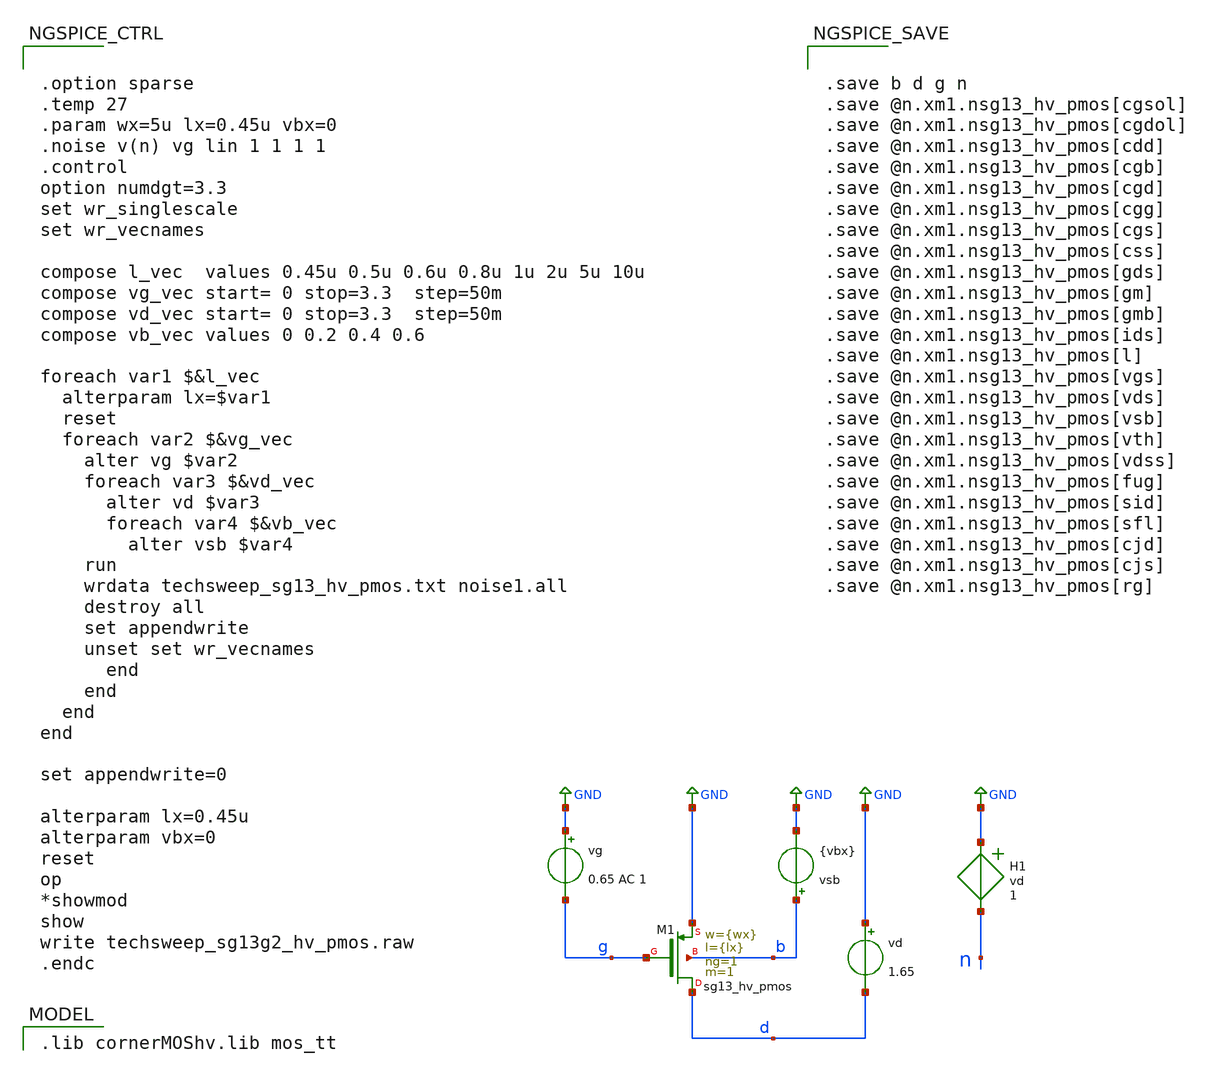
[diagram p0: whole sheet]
** sch_path: 3_real_circuits/techsweep_sg13g2_hv_pmos_test.sch
**.subckt techsweep_sg13g2_hv_pmos_test
XM1 d g GND b sg13_hv_pmos w={wx} l={lx} ng=1 m=1 mm_ok=1
vd GND d 1.65
vsb b GND {vbx}
vg GND g 0.65 AC 1
H1 GND n vd 1
**** begin user architecture code
 .lib cornerMOShv.lib mos_tt



.save b d g n
.save @n.xm1.nsg13_hv_pmos[cgsol]
.save @n.xm1.nsg13_hv_pmos[cgdol]
.save @n.xm1.nsg13_hv_pmos[cdd]
.save @n.xm1.nsg13_hv_pmos[cgb]
.save @n.xm1.nsg13_hv_pmos[cgd]
.save @n.xm1.nsg13_hv_pmos[cgg]
.save @n.xm1.nsg13_hv_pmos[cgs]
.save @n.xm1.nsg13_hv_pmos[css]
.save @n.xm1.nsg13_hv_pmos[gds]
.save @n.xm1.nsg13_hv_pmos[gm]
.save @n.xm1.nsg13_hv_pmos[gmb]
.save @n.xm1.nsg13_hv_pmos[ids]
.save @n.xm1.nsg13_hv_pmos[l]
.save @n.xm1.nsg13_hv_pmos[vgs]
.save @n.xm1.nsg13_hv_pmos[vds]
.save @n.xm1.nsg13_hv_pmos[vsb]
.save @n.xm1.nsg13_hv_pmos[vth]
.save @n.xm1.nsg13_hv_pmos[vdss]
.save @n.xm1.nsg13_hv_pmos[fug]
.save @n.xm1.nsg13_hv_pmos[sid]
.save @n.xm1.nsg13_hv_pmos[sfl]
.save @n.xm1.nsg13_hv_pmos[cjd]
.save @n.xm1.nsg13_hv_pmos[cjs]
.save @n.xm1.nsg13_hv_pmos[rg]




.option sparse
.temp 27
.param wx=5u lx=0.45u vbx=0
.noise v(n) vg lin 1 1 1 1
.control
option numdgt=3.3
set wr_singlescale
set wr_vecnames

compose l_vec  values 0.45u 0.5u 0.6u 0.8u 1u 2u 5u 10u
compose vg_vec start= 0 stop=3.3  step=50m
compose vd_vec start= 0 stop=3.3  step=50m
compose vb_vec values 0 0.2 0.4 0.6

foreach var1 $&l_vec
  alterparam lx=$var1
  reset
  foreach var2 $&vg_vec
    alter vg $var2
    foreach var3 $&vd_vec
      alter vd $var3
      foreach var4 $&vb_vec
        alter vsb $var4
	run
	wrdata techsweep_sg13_hv_pmos.txt noise1.all
	destroy all
	set appendwrite
	unset set wr_vecnames
      end
    end
  end
end

set appendwrite=0

alterparam lx=0.45u
alterparam vbx=0
reset
op
*showmod
show
write techsweep_sg13g2_hv_pmos.raw
.endc


**** end user architecture code
**.ends
.GLOBAL GND
.end
